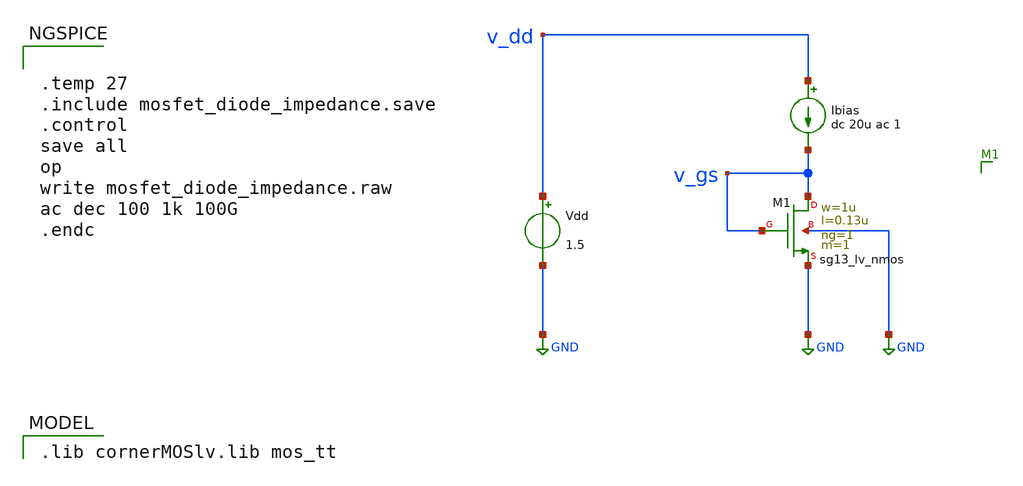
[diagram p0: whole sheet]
** sch_path: xschem/mosfet_diode_impedance.sch
* (c) 2024-2025 Harald Pretl, Apache-2.0 license
**.subckt mosfet_diode_impedance
Vdd v_dd GND 1.5
XM1 v_gs v_gs GND GND sg13_lv_nmos w=1u l=0.13u ng=1 m=1 mm_ok=1
Ibias v_dd v_gs dc 20u ac 1
**** begin user architecture code
 .lib cornerMOSlv.lib mos_tt



.temp 27
.include mosfet_diode_impedance.save
.control
save all
op
write mosfet_diode_impedance.raw
ac dec 100 1k 100G
.endc


**** end user architecture code
**.ends
.GLOBAL GND
.end
